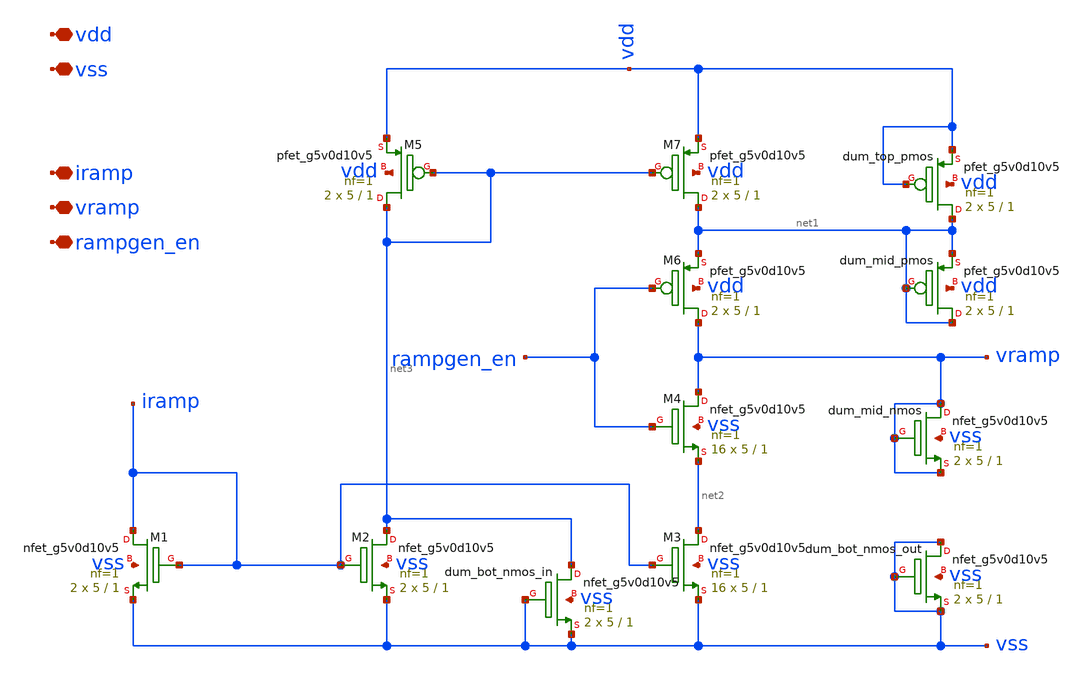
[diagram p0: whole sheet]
** sch_path: design/oscillator/rampgen_w_dummies.sch
**.subckt rampgen_w_dummies vdd vss iramp vramp rampgen_en
*.iopin vdd
*.iopin vss
*.iopin iramp
*.iopin vramp
*.iopin rampgen_en
XM1 iramp iramp vss vss sky130_fd_pr__nfet_g5v0d10v5 L=1 W=5 nf=1 ad='int((nf+1)/2) * W/nf * 0.29' as='int((nf+2)/2) * W/nf * 0.29'
+ pd='2*int((nf+1)/2) * (W/nf + 0.29)' ps='2*int((nf+2)/2) * (W/nf + 0.29)' nrd='0.29 / W' nrs='0.29 / W'
+ sa=0 sb=0 sd=0 mult=2 m=2
XM2 net3 iramp vss vss sky130_fd_pr__nfet_g5v0d10v5 L=1 W=5 nf=1 ad='int((nf+1)/2) * W/nf * 0.29' as='int((nf+2)/2) * W/nf * 0.29'
+ pd='2*int((nf+1)/2) * (W/nf + 0.29)' ps='2*int((nf+2)/2) * (W/nf + 0.29)' nrd='0.29 / W' nrs='0.29 / W'
+ sa=0 sb=0 sd=0 mult=2 m=2
XM3 net2 iramp vss vss sky130_fd_pr__nfet_g5v0d10v5 L=1 W=5 nf=1 ad='int((nf+1)/2) * W/nf * 0.29' as='int((nf+2)/2) * W/nf * 0.29'
+ pd='2*int((nf+1)/2) * (W/nf + 0.29)' ps='2*int((nf+2)/2) * (W/nf + 0.29)' nrd='0.29 / W' nrs='0.29 / W'
+ sa=0 sb=0 sd=0 mult=16 m=16
XM4 vramp rampgen_en net2 vss sky130_fd_pr__nfet_g5v0d10v5 L=1 W=5 nf=1 ad='int((nf+1)/2) * W/nf * 0.29'
+ as='int((nf+2)/2) * W/nf * 0.29' pd='2*int((nf+1)/2) * (W/nf + 0.29)' ps='2*int((nf+2)/2) * (W/nf + 0.29)'
+ nrd='0.29 / W' nrs='0.29 / W' sa=0 sb=0 sd=0 mult=16 m=16
XM5 net3 net3 vdd vdd sky130_fd_pr__pfet_g5v0d10v5 L=1 W=5 nf=1 ad='int((nf+1)/2) * W/nf * 0.29' as='int((nf+2)/2) * W/nf * 0.29'
+ pd='2*int((nf+1)/2) * (W/nf + 0.29)' ps='2*int((nf+2)/2) * (W/nf + 0.29)' nrd='0.29 / W' nrs='0.29 / W'
+ sa=0 sb=0 sd=0 mult=2 m=2
XM6 vramp rampgen_en net1 vdd sky130_fd_pr__pfet_g5v0d10v5 L=1 W=5 nf=1 ad='int((nf+1)/2) * W/nf * 0.29'
+ as='int((nf+2)/2) * W/nf * 0.29' pd='2*int((nf+1)/2) * (W/nf + 0.29)' ps='2*int((nf+2)/2) * (W/nf + 0.29)'
+ nrd='0.29 / W' nrs='0.29 / W' sa=0 sb=0 sd=0 mult=2 m=2
XM7 net1 net3 vdd vdd sky130_fd_pr__pfet_g5v0d10v5 L=1 W=5 nf=1 ad='int((nf+1)/2) * W/nf * 0.29' as='int((nf+2)/2) * W/nf * 0.29'
+ pd='2*int((nf+1)/2) * (W/nf + 0.29)' ps='2*int((nf+2)/2) * (W/nf + 0.29)' nrd='0.29 / W' nrs='0.29 / W'
+ sa=0 sb=0 sd=0 mult=2 m=2
Xdum_top_pmos net1 vdd vdd vdd sky130_fd_pr__pfet_g5v0d10v5 L=1 W=5 nf=1 ad='int((nf+1)/2) * W/nf * 0.29'
+ as='int((nf+2)/2) * W/nf * 0.29' pd='2*int((nf+1)/2) * (W/nf + 0.29)' ps='2*int((nf+2)/2) * (W/nf + 0.29)'
+ nrd='0.29 / W' nrs='0.29 / W' sa=0 sb=0 sd=0 mult=2 m=2
Xdum_mid_pmos net1 net1 net1 vdd sky130_fd_pr__pfet_g5v0d10v5 L=1 W=5 nf=1 ad='int((nf+1)/2) * W/nf * 0.29'
+ as='int((nf+2)/2) * W/nf * 0.29' pd='2*int((nf+1)/2) * (W/nf + 0.29)' ps='2*int((nf+2)/2) * (W/nf + 0.29)'
+ nrd='0.29 / W' nrs='0.29 / W' sa=0 sb=0 sd=0 mult=2 m=2
Xdum_mid_nmos vramp vramp vramp vss sky130_fd_pr__nfet_g5v0d10v5 L=1 W=5 nf=1 ad='int((nf+1)/2) * W/nf * 0.29'
+ as='int((nf+2)/2) * W/nf * 0.29' pd='2*int((nf+1)/2) * (W/nf + 0.29)' ps='2*int((nf+2)/2) * (W/nf + 0.29)'
+ nrd='0.29 / W' nrs='0.29 / W' sa=0 sb=0 sd=0 mult=2 m=2
Xdum_bot_nmos_out vss vss vss vss sky130_fd_pr__nfet_g5v0d10v5 L=1 W=5 nf=1 ad='int((nf+1)/2) * W/nf * 0.29'
+ as='int((nf+2)/2) * W/nf * 0.29' pd='2*int((nf+1)/2) * (W/nf + 0.29)' ps='2*int((nf+2)/2) * (W/nf + 0.29)'
+ nrd='0.29 / W' nrs='0.29 / W' sa=0 sb=0 sd=0 mult=2 m=2
Xdum_bot_nmos_in net3 vss vss vss sky130_fd_pr__nfet_g5v0d10v5 L=1 W=5 nf=1 ad='int((nf+1)/2) * W/nf * 0.29'
+ as='int((nf+2)/2) * W/nf * 0.29' pd='2*int((nf+1)/2) * (W/nf + 0.29)' ps='2*int((nf+2)/2) * (W/nf + 0.29)'
+ nrd='0.29 / W' nrs='0.29 / W' sa=0 sb=0 sd=0 mult=2 m=2
**.ends
.end
